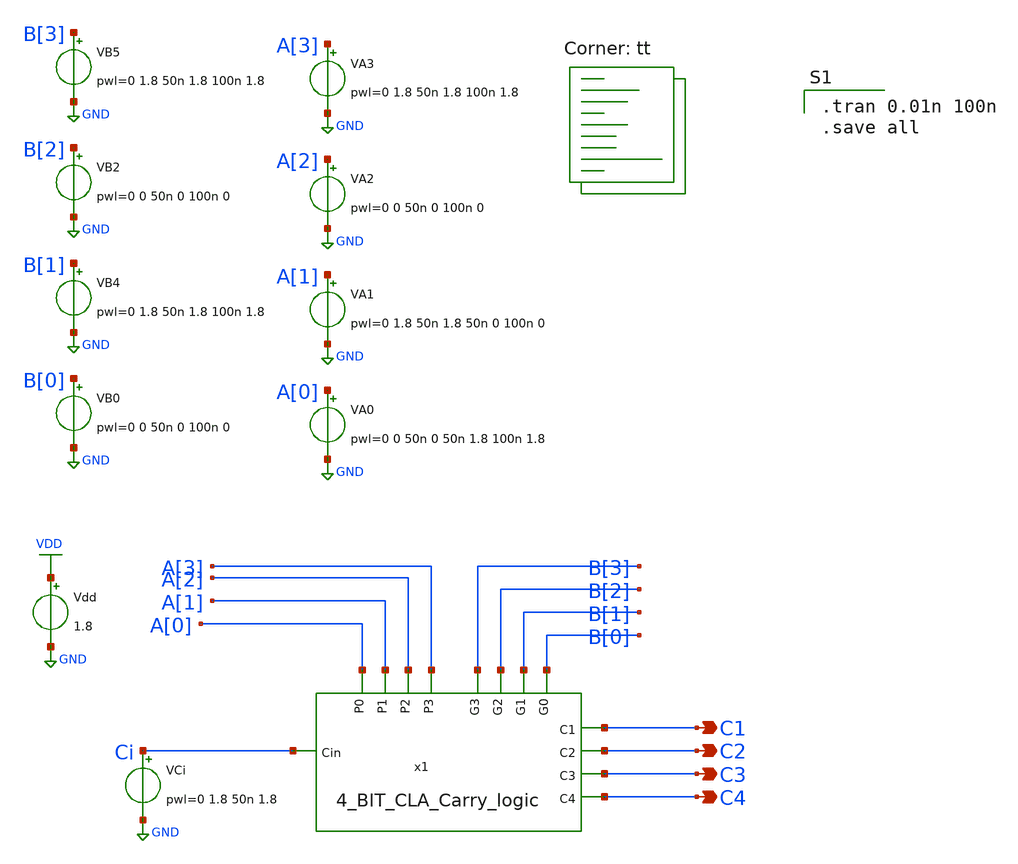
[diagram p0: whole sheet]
** sch_path: gates/cla logicsim.sch
**.subckt cla logicsim C4 C3 C2 C1
*.opin C4
*.opin C3
*.opin C2
*.opin C1
x1 A[1] B[1] A[3] A[0] A[2] B[2] B[3] Ci B[0] C1 C2 C3 C4 4_BIT_CLA_Carry_logic
VA3 A[3] GND pwl=0 1.8 50n 1.8 100n 1.8
VA2 A[2] GND pwl=0 0 50n 0 100n 0
VA1 A[1] GND pwl=0 1.8 50n 1.8 50n 0 100n 0
VA0 A[0] GND pwl=0 0 50n 0 50n 1.8 100n 1.8
VB5 B[3] GND pwl=0 1.8 50n 1.8 100n 1.8
VB2 B[2] GND pwl=0 0 50n 0 100n 0
VB4 B[1] GND pwl=0 1.8 50n 1.8 100n 1.8
VB0 B[0] GND pwl=0 0 50n 0 100n 0
VCi Ci GND pwl=0 1.8 50n 1.8
Vdd VDD GND 1.8
**** begin user architecture code
.lib $::SKYWATER_MODELS/sky130.lib.spice tt

.tran 0.01n 100n
.save all

**** end user architecture code
**.ends

* expanding   symbol:  4_BIT_CLA_Carry_logic.sym # of pins=13
** sym_path: gates/4_BIT_CLA_Carry_logic.sym
** sch_path: gates/4_BIT_CLA_Carry_logic.sch
.subckt 4_BIT_CLA_Carry_logic P1 G1 P3 P0 P2 G2 G3 Cin G0 C1 C2 C3 C4
*.ipin P0
*.ipin P1
*.ipin P2
*.ipin P3
*.ipin G0
*.ipin G1
*.ipin G2
*.ipin G3
*.ipin Cin
*.opin C1
*.opin C2
*.opin C3
*.opin C4
x5 Cin x5 P0 AND2
x6 G0 C1 x5 OR2
x7 G1 net1 net2 C2 OR3
x8 P1 net1 G0 AND2
x9 Cin net10 P0 P1 AND3
x1 G2 net3 net4 C3 net5 OR4
x2 P2 net3 G1 AND2
x3 P1 net11 P2 G0 AND3
x4 net12 net5 net13 net14 net15 AND4
x10 G3 net6 net7 net8 C4 net9 OR5
x12 P3 net6 G2 AND2
x13 net16 net17 net18 net19 AND3
x14 net20 net8 net21 net22 net23 AND4
x11 net24 net25 net26 net27 net28 net29 AND5
.ends


* expanding   symbol:  AND2.sym # of pins=3
** sym_path: gates/AND2.sym
** sch_path: gates/AND2.sch
.subckt AND2 A Y B
*.opin Y
*.ipin A
*.ipin B
x1 A net1 B NAND2_Gate
X2 net1 Y inv_vtc
.ends


* expanding   symbol:  OR2.sym # of pins=3
** sym_path: gates/OR2.sym
** sch_path: gates/OR2.sch
.subckt OR2 B Y A
*.ipin A
*.ipin B
*.opin Y
XM7 VDD B net2 VDD sky130_fd_pr__pfet_01v8 L=0.15 W=1 nf=1 ad='int((nf+1)/2) * W/nf * 0.29' as='int((nf+2)/2) * W/nf * 0.29'
+ pd='2*int((nf+1)/2) * (W/nf + 0.29)' ps='2*int((nf+2)/2) * (W/nf + 0.29)' nrd='0.29 / W' nrs='0.29 / W'
+ sa=0 sb=0 sd=0 mult=1 m=1
XM8 GND B net1 GND sky130_fd_pr__nfet_01v8 L=0.15 W=1 nf=1 ad='int((nf+1)/2) * W/nf * 0.29' as='int((nf+2)/2) * W/nf * 0.29'
+ pd='2*int((nf+1)/2) * (W/nf + 0.29)' ps='2*int((nf+2)/2) * (W/nf + 0.29)' nrd='0.29 / W' nrs='0.29 / W'
+ sa=0 sb=0 sd=0 mult=1 m=1
XM9 net2 A net1 VDD sky130_fd_pr__pfet_01v8 L=0.15 W=1 nf=1 ad='int((nf+1)/2) * W/nf * 0.29' as='int((nf+2)/2) * W/nf * 0.29'
+ pd='2*int((nf+1)/2) * (W/nf + 0.29)' ps='2*int((nf+2)/2) * (W/nf + 0.29)' nrd='0.29 / W' nrs='0.29 / W'
+ sa=0 sb=0 sd=0 mult=1 m=1
XM10 GND A net1 GND sky130_fd_pr__nfet_01v8 L=0.15 W=1 nf=1 ad='int((nf+1)/2) * W/nf * 0.29' as='int((nf+2)/2) * W/nf * 0.29'
+ pd='2*int((nf+1)/2) * (W/nf + 0.29)' ps='2*int((nf+2)/2) * (W/nf + 0.29)' nrd='0.29 / W' nrs='0.29 / W'
+ sa=0 sb=0 sd=0 mult=1 m=1
X1 net1 Y inv_vtc
.ends


* expanding   symbol:  OR3.sym # of pins=4
** sym_path: gates/OR3.sym
** sch_path: gates/OR3.sch
.subckt OR3 C B A Y
*.ipin A
*.ipin B
*.opin Y
*.ipin C
XM5 VDD C net3 VDD sky130_fd_pr__pfet_01v8 L=0.15 W=1 nf=1 ad='int((nf+1)/2) * W/nf * 0.29' as='int((nf+2)/2) * W/nf * 0.29'
+ pd='2*int((nf+1)/2) * (W/nf + 0.29)' ps='2*int((nf+2)/2) * (W/nf + 0.29)' nrd='0.29 / W' nrs='0.29 / W'
+ sa=0 sb=0 sd=0 mult=1 m=1
XM6 GND C net1 GND sky130_fd_pr__nfet_01v8 L=0.15 W=1 nf=1 ad='int((nf+1)/2) * W/nf * 0.29' as='int((nf+2)/2) * W/nf * 0.29'
+ pd='2*int((nf+1)/2) * (W/nf + 0.29)' ps='2*int((nf+2)/2) * (W/nf + 0.29)' nrd='0.29 / W' nrs='0.29 / W'
+ sa=0 sb=0 sd=0 mult=1 m=1
XM7 net3 B net2 VDD sky130_fd_pr__pfet_01v8 L=0.15 W=1 nf=1 ad='int((nf+1)/2) * W/nf * 0.29' as='int((nf+2)/2) * W/nf * 0.29'
+ pd='2*int((nf+1)/2) * (W/nf + 0.29)' ps='2*int((nf+2)/2) * (W/nf + 0.29)' nrd='0.29 / W' nrs='0.29 / W'
+ sa=0 sb=0 sd=0 mult=1 m=1
XM8 GND B net1 GND sky130_fd_pr__nfet_01v8 L=0.15 W=1 nf=1 ad='int((nf+1)/2) * W/nf * 0.29' as='int((nf+2)/2) * W/nf * 0.29'
+ pd='2*int((nf+1)/2) * (W/nf + 0.29)' ps='2*int((nf+2)/2) * (W/nf + 0.29)' nrd='0.29 / W' nrs='0.29 / W'
+ sa=0 sb=0 sd=0 mult=1 m=1
XM9 net2 A net1 VDD sky130_fd_pr__pfet_01v8 L=0.15 W=1 nf=1 ad='int((nf+1)/2) * W/nf * 0.29' as='int((nf+2)/2) * W/nf * 0.29'
+ pd='2*int((nf+1)/2) * (W/nf + 0.29)' ps='2*int((nf+2)/2) * (W/nf + 0.29)' nrd='0.29 / W' nrs='0.29 / W'
+ sa=0 sb=0 sd=0 mult=1 m=1
XM10 GND A net1 GND sky130_fd_pr__nfet_01v8 L=0.15 W=1 nf=1 ad='int((nf+1)/2) * W/nf * 0.29' as='int((nf+2)/2) * W/nf * 0.29'
+ pd='2*int((nf+1)/2) * (W/nf + 0.29)' ps='2*int((nf+2)/2) * (W/nf + 0.29)' nrd='0.29 / W' nrs='0.29 / W'
+ sa=0 sb=0 sd=0 mult=1 m=1
X1 net1 Y inv_vtc
.ends


* expanding   symbol:  AND3.sym # of pins=4
** sym_path: gates/AND3.sym
** sch_path: gates/AND3.sch
.subckt AND3 A Y B c
*.ipin A
*.ipin B
*.opin Y
*.ipin c
XM1 net1 A net2 GND sky130_fd_pr__nfet_01v8 L=0.15 W=1 nf=1 ad='int((nf+1)/2) * W/nf * 0.29' as='int((nf+2)/2) * W/nf * 0.29'
+ pd='2*int((nf+1)/2) * (W/nf + 0.29)' ps='2*int((nf+2)/2) * (W/nf + 0.29)' nrd='0.29 / W' nrs='0.29 / W'
+ sa=0 sb=0 sd=0 mult=1 m=1
XM2 net2 B net3 GND sky130_fd_pr__nfet_01v8 L=0.15 W=1 nf=1 ad='int((nf+1)/2) * W/nf * 0.29' as='int((nf+2)/2) * W/nf * 0.29'
+ pd='2*int((nf+1)/2) * (W/nf + 0.29)' ps='2*int((nf+2)/2) * (W/nf + 0.29)' nrd='0.29 / W' nrs='0.29 / W'
+ sa=0 sb=0 sd=0 mult=1 m=1
XM3 net1 A VDD VDD sky130_fd_pr__pfet_01v8 L=0.15 W=1 nf=1 ad='int((nf+1)/2) * W/nf * 0.29' as='int((nf+2)/2) * W/nf * 0.29'
+ pd='2*int((nf+1)/2) * (W/nf + 0.29)' ps='2*int((nf+2)/2) * (W/nf + 0.29)' nrd='0.29 / W' nrs='0.29 / W'
+ sa=0 sb=0 sd=0 mult=1 m=1
XM4 net1 B VDD VDD sky130_fd_pr__pfet_01v8 L=0.15 W=1 nf=1 ad='int((nf+1)/2) * W/nf * 0.29' as='int((nf+2)/2) * W/nf * 0.29'
+ pd='2*int((nf+1)/2) * (W/nf + 0.29)' ps='2*int((nf+2)/2) * (W/nf + 0.29)' nrd='0.29 / W' nrs='0.29 / W'
+ sa=0 sb=0 sd=0 mult=1 m=1
XM5 net1 c VDD VDD sky130_fd_pr__pfet_01v8 L=0.15 W=1 nf=1 ad='int((nf+1)/2) * W/nf * 0.29' as='int((nf+2)/2) * W/nf * 0.29'
+ pd='2*int((nf+1)/2) * (W/nf + 0.29)' ps='2*int((nf+2)/2) * (W/nf + 0.29)' nrd='0.29 / W' nrs='0.29 / W'
+ sa=0 sb=0 sd=0 mult=1 m=1
XM6 net3 c GND GND sky130_fd_pr__nfet_01v8 L=0.15 W=1 nf=1 ad='int((nf+1)/2) * W/nf * 0.29' as='int((nf+2)/2) * W/nf * 0.29'
+ pd='2*int((nf+1)/2) * (W/nf + 0.29)' ps='2*int((nf+2)/2) * (W/nf + 0.29)' nrd='0.29 / W' nrs='0.29 / W'
+ sa=0 sb=0 sd=0 mult=1 m=1
X1 net1 Y inv_vtc
.ends


* expanding   symbol:  OR4.sym # of pins=5
** sym_path: gates/OR4.sym
** sch_path: gates/OR4.sch
.subckt OR4 D C B Y A
*.ipin A
*.ipin B
*.opin Y
*.ipin C
*.ipin D
XM2 GND D net1 GND sky130_fd_pr__nfet_01v8 L=0.15 W=1 nf=1 ad='int((nf+1)/2) * W/nf * 0.29' as='int((nf+2)/2) * W/nf * 0.29'
+ pd='2*int((nf+1)/2) * (W/nf + 0.29)' ps='2*int((nf+2)/2) * (W/nf + 0.29)' nrd='0.29 / W' nrs='0.29 / W'
+ sa=0 sb=0 sd=0 mult=1 m=1
XM4 VDD D net4 VDD sky130_fd_pr__pfet_01v8 L=0.15 W=1 nf=1 ad='int((nf+1)/2) * W/nf * 0.29' as='int((nf+2)/2) * W/nf * 0.29'
+ pd='2*int((nf+1)/2) * (W/nf + 0.29)' ps='2*int((nf+2)/2) * (W/nf + 0.29)' nrd='0.29 / W' nrs='0.29 / W'
+ sa=0 sb=0 sd=0 mult=1 m=1
XM5 net4 C net3 VDD sky130_fd_pr__pfet_01v8 L=0.15 W=1 nf=1 ad='int((nf+1)/2) * W/nf * 0.29' as='int((nf+2)/2) * W/nf * 0.29'
+ pd='2*int((nf+1)/2) * (W/nf + 0.29)' ps='2*int((nf+2)/2) * (W/nf + 0.29)' nrd='0.29 / W' nrs='0.29 / W'
+ sa=0 sb=0 sd=0 mult=1 m=1
XM6 GND C net1 GND sky130_fd_pr__nfet_01v8 L=0.15 W=1 nf=1 ad='int((nf+1)/2) * W/nf * 0.29' as='int((nf+2)/2) * W/nf * 0.29'
+ pd='2*int((nf+1)/2) * (W/nf + 0.29)' ps='2*int((nf+2)/2) * (W/nf + 0.29)' nrd='0.29 / W' nrs='0.29 / W'
+ sa=0 sb=0 sd=0 mult=1 m=1
XM7 net3 B net2 VDD sky130_fd_pr__pfet_01v8 L=0.15 W=1 nf=1 ad='int((nf+1)/2) * W/nf * 0.29' as='int((nf+2)/2) * W/nf * 0.29'
+ pd='2*int((nf+1)/2) * (W/nf + 0.29)' ps='2*int((nf+2)/2) * (W/nf + 0.29)' nrd='0.29 / W' nrs='0.29 / W'
+ sa=0 sb=0 sd=0 mult=1 m=1
XM8 GND B net1 GND sky130_fd_pr__nfet_01v8 L=0.15 W=1 nf=1 ad='int((nf+1)/2) * W/nf * 0.29' as='int((nf+2)/2) * W/nf * 0.29'
+ pd='2*int((nf+1)/2) * (W/nf + 0.29)' ps='2*int((nf+2)/2) * (W/nf + 0.29)' nrd='0.29 / W' nrs='0.29 / W'
+ sa=0 sb=0 sd=0 mult=1 m=1
XM9 net2 A net1 VDD sky130_fd_pr__pfet_01v8 L=0.15 W=1 nf=1 ad='int((nf+1)/2) * W/nf * 0.29' as='int((nf+2)/2) * W/nf * 0.29'
+ pd='2*int((nf+1)/2) * (W/nf + 0.29)' ps='2*int((nf+2)/2) * (W/nf + 0.29)' nrd='0.29 / W' nrs='0.29 / W'
+ sa=0 sb=0 sd=0 mult=1 m=1
XM10 GND A net1 GND sky130_fd_pr__nfet_01v8 L=0.15 W=1 nf=1 ad='int((nf+1)/2) * W/nf * 0.29' as='int((nf+2)/2) * W/nf * 0.29'
+ pd='2*int((nf+1)/2) * (W/nf + 0.29)' ps='2*int((nf+2)/2) * (W/nf + 0.29)' nrd='0.29 / W' nrs='0.29 / W'
+ sa=0 sb=0 sd=0 mult=1 m=1
X2 net1 Y inv_vtc
.ends


* expanding   symbol:  AND4.sym # of pins=5
** sym_path: gates/AND4.sym
** sch_path: gates/AND4.sch
.subckt AND4 A Y B C D
*.ipin A
*.ipin B
*.opin Y
*.ipin C
*.ipin D
XM1 net1 A net2 GND sky130_fd_pr__nfet_01v8 L=0.15 W=1 nf=1 ad='int((nf+1)/2) * W/nf * 0.29' as='int((nf+2)/2) * W/nf * 0.29'
+ pd='2*int((nf+1)/2) * (W/nf + 0.29)' ps='2*int((nf+2)/2) * (W/nf + 0.29)' nrd='0.29 / W' nrs='0.29 / W'
+ sa=0 sb=0 sd=0 mult=1 m=1
XM2 net2 B net3 GND sky130_fd_pr__nfet_01v8 L=0.15 W=1 nf=1 ad='int((nf+1)/2) * W/nf * 0.29' as='int((nf+2)/2) * W/nf * 0.29'
+ pd='2*int((nf+1)/2) * (W/nf + 0.29)' ps='2*int((nf+2)/2) * (W/nf + 0.29)' nrd='0.29 / W' nrs='0.29 / W'
+ sa=0 sb=0 sd=0 mult=1 m=1
XM3 net1 A VDD VDD sky130_fd_pr__pfet_01v8 L=0.15 W=1 nf=1 ad='int((nf+1)/2) * W/nf * 0.29' as='int((nf+2)/2) * W/nf * 0.29'
+ pd='2*int((nf+1)/2) * (W/nf + 0.29)' ps='2*int((nf+2)/2) * (W/nf + 0.29)' nrd='0.29 / W' nrs='0.29 / W'
+ sa=0 sb=0 sd=0 mult=1 m=1
XM4 net1 B VDD VDD sky130_fd_pr__pfet_01v8 L=0.15 W=1 nf=1 ad='int((nf+1)/2) * W/nf * 0.29' as='int((nf+2)/2) * W/nf * 0.29'
+ pd='2*int((nf+1)/2) * (W/nf + 0.29)' ps='2*int((nf+2)/2) * (W/nf + 0.29)' nrd='0.29 / W' nrs='0.29 / W'
+ sa=0 sb=0 sd=0 mult=1 m=1
XM5 net1 C VDD VDD sky130_fd_pr__pfet_01v8 L=0.15 W=1 nf=1 ad='int((nf+1)/2) * W/nf * 0.29' as='int((nf+2)/2) * W/nf * 0.29'
+ pd='2*int((nf+1)/2) * (W/nf + 0.29)' ps='2*int((nf+2)/2) * (W/nf + 0.29)' nrd='0.29 / W' nrs='0.29 / W'
+ sa=0 sb=0 sd=0 mult=1 m=1
XM6 net3 C net4 GND sky130_fd_pr__nfet_01v8 L=0.15 W=1 nf=1 ad='int((nf+1)/2) * W/nf * 0.29' as='int((nf+2)/2) * W/nf * 0.29'
+ pd='2*int((nf+1)/2) * (W/nf + 0.29)' ps='2*int((nf+2)/2) * (W/nf + 0.29)' nrd='0.29 / W' nrs='0.29 / W'
+ sa=0 sb=0 sd=0 mult=1 m=1
XM7 net1 D VDD VDD sky130_fd_pr__pfet_01v8 L=0.15 W=1 nf=1 ad='int((nf+1)/2) * W/nf * 0.29' as='int((nf+2)/2) * W/nf * 0.29'
+ pd='2*int((nf+1)/2) * (W/nf + 0.29)' ps='2*int((nf+2)/2) * (W/nf + 0.29)' nrd='0.29 / W' nrs='0.29 / W'
+ sa=0 sb=0 sd=0 mult=1 m=1
XM8 net4 D GND GND sky130_fd_pr__nfet_01v8 L=0.15 W=1 nf=1 ad='int((nf+1)/2) * W/nf * 0.29' as='int((nf+2)/2) * W/nf * 0.29'
+ pd='2*int((nf+1)/2) * (W/nf + 0.29)' ps='2*int((nf+2)/2) * (W/nf + 0.29)' nrd='0.29 / W' nrs='0.29 / W'
+ sa=0 sb=0 sd=0 mult=1 m=1
X1 net1 Y inv_vtc
.ends


* expanding   symbol:  OR5.sym # of pins=6
** sym_path: gates/OR5.sym
** sch_path: gates/OR5.sch
.subckt OR5 E D C B Y A
*.ipin A
*.ipin B
*.opin Y
*.ipin C
*.ipin D
*.ipin E
XM1 GND E net1 GND sky130_fd_pr__nfet_01v8 L=0.15 W=1 nf=1 ad='int((nf+1)/2) * W/nf * 0.29' as='int((nf+2)/2) * W/nf * 0.29'
+ pd='2*int((nf+1)/2) * (W/nf + 0.29)' ps='2*int((nf+2)/2) * (W/nf + 0.29)' nrd='0.29 / W' nrs='0.29 / W'
+ sa=0 sb=0 sd=0 mult=1 m=1
XM2 GND D net1 GND sky130_fd_pr__nfet_01v8 L=0.15 W=1 nf=1 ad='int((nf+1)/2) * W/nf * 0.29' as='int((nf+2)/2) * W/nf * 0.29'
+ pd='2*int((nf+1)/2) * (W/nf + 0.29)' ps='2*int((nf+2)/2) * (W/nf + 0.29)' nrd='0.29 / W' nrs='0.29 / W'
+ sa=0 sb=0 sd=0 mult=1 m=1
XM3 VDD E VDD VDD sky130_fd_pr__pfet_01v8 L=0.15 W=1 nf=1 ad='int((nf+1)/2) * W/nf * 0.29' as='int((nf+2)/2) * W/nf * 0.29'
+ pd='2*int((nf+1)/2) * (W/nf + 0.29)' ps='2*int((nf+2)/2) * (W/nf + 0.29)' nrd='0.29 / W' nrs='0.29 / W'
+ sa=0 sb=0 sd=0 mult=1 m=1
XM4 VDD D net4 VDD sky130_fd_pr__pfet_01v8 L=0.15 W=1 nf=1 ad='int((nf+1)/2) * W/nf * 0.29' as='int((nf+2)/2) * W/nf * 0.29'
+ pd='2*int((nf+1)/2) * (W/nf + 0.29)' ps='2*int((nf+2)/2) * (W/nf + 0.29)' nrd='0.29 / W' nrs='0.29 / W'
+ sa=0 sb=0 sd=0 mult=1 m=1
XM5 net4 C net3 VDD sky130_fd_pr__pfet_01v8 L=0.15 W=1 nf=1 ad='int((nf+1)/2) * W/nf * 0.29' as='int((nf+2)/2) * W/nf * 0.29'
+ pd='2*int((nf+1)/2) * (W/nf + 0.29)' ps='2*int((nf+2)/2) * (W/nf + 0.29)' nrd='0.29 / W' nrs='0.29 / W'
+ sa=0 sb=0 sd=0 mult=1 m=1
XM6 GND C net1 GND sky130_fd_pr__nfet_01v8 L=0.15 W=1 nf=1 ad='int((nf+1)/2) * W/nf * 0.29' as='int((nf+2)/2) * W/nf * 0.29'
+ pd='2*int((nf+1)/2) * (W/nf + 0.29)' ps='2*int((nf+2)/2) * (W/nf + 0.29)' nrd='0.29 / W' nrs='0.29 / W'
+ sa=0 sb=0 sd=0 mult=1 m=1
XM7 net3 B net2 VDD sky130_fd_pr__pfet_01v8 L=0.15 W=1 nf=1 ad='int((nf+1)/2) * W/nf * 0.29' as='int((nf+2)/2) * W/nf * 0.29'
+ pd='2*int((nf+1)/2) * (W/nf + 0.29)' ps='2*int((nf+2)/2) * (W/nf + 0.29)' nrd='0.29 / W' nrs='0.29 / W'
+ sa=0 sb=0 sd=0 mult=1 m=1
XM8 GND B net1 GND sky130_fd_pr__nfet_01v8 L=0.15 W=1 nf=1 ad='int((nf+1)/2) * W/nf * 0.29' as='int((nf+2)/2) * W/nf * 0.29'
+ pd='2*int((nf+1)/2) * (W/nf + 0.29)' ps='2*int((nf+2)/2) * (W/nf + 0.29)' nrd='0.29 / W' nrs='0.29 / W'
+ sa=0 sb=0 sd=0 mult=1 m=1
XM9 net2 A net1 VDD sky130_fd_pr__pfet_01v8 L=0.15 W=1 nf=1 ad='int((nf+1)/2) * W/nf * 0.29' as='int((nf+2)/2) * W/nf * 0.29'
+ pd='2*int((nf+1)/2) * (W/nf + 0.29)' ps='2*int((nf+2)/2) * (W/nf + 0.29)' nrd='0.29 / W' nrs='0.29 / W'
+ sa=0 sb=0 sd=0 mult=1 m=1
XM10 GND A net1 GND sky130_fd_pr__nfet_01v8 L=0.15 W=1 nf=1 ad='int((nf+1)/2) * W/nf * 0.29' as='int((nf+2)/2) * W/nf * 0.29'
+ pd='2*int((nf+1)/2) * (W/nf + 0.29)' ps='2*int((nf+2)/2) * (W/nf + 0.29)' nrd='0.29 / W' nrs='0.29 / W'
+ sa=0 sb=0 sd=0 mult=1 m=1
X2 net1 Y inv_vtc
.ends


* expanding   symbol:  AND5.sym # of pins=6
** sym_path: gates/AND5.sym
** sch_path: gates/AND5.sch
.subckt AND5 A Y B C D E
*.ipin A
*.ipin B
*.opin Y
*.ipin C
*.ipin D
*.ipin E
XM1 net1 A net2 GND sky130_fd_pr__nfet_01v8 L=0.15 W=1 nf=1 ad='int((nf+1)/2) * W/nf * 0.29' as='int((nf+2)/2) * W/nf * 0.29'
+ pd='2*int((nf+1)/2) * (W/nf + 0.29)' ps='2*int((nf+2)/2) * (W/nf + 0.29)' nrd='0.29 / W' nrs='0.29 / W'
+ sa=0 sb=0 sd=0 mult=1 m=1
XM2 net2 B net3 GND sky130_fd_pr__nfet_01v8 L=0.15 W=1 nf=1 ad='int((nf+1)/2) * W/nf * 0.29' as='int((nf+2)/2) * W/nf * 0.29'
+ pd='2*int((nf+1)/2) * (W/nf + 0.29)' ps='2*int((nf+2)/2) * (W/nf + 0.29)' nrd='0.29 / W' nrs='0.29 / W'
+ sa=0 sb=0 sd=0 mult=1 m=1
XM3 net1 A VDD VDD sky130_fd_pr__pfet_01v8 L=0.15 W=1 nf=1 ad='int((nf+1)/2) * W/nf * 0.29' as='int((nf+2)/2) * W/nf * 0.29'
+ pd='2*int((nf+1)/2) * (W/nf + 0.29)' ps='2*int((nf+2)/2) * (W/nf + 0.29)' nrd='0.29 / W' nrs='0.29 / W'
+ sa=0 sb=0 sd=0 mult=1 m=1
XM4 net1 B VDD VDD sky130_fd_pr__pfet_01v8 L=0.15 W=1 nf=1 ad='int((nf+1)/2) * W/nf * 0.29' as='int((nf+2)/2) * W/nf * 0.29'
+ pd='2*int((nf+1)/2) * (W/nf + 0.29)' ps='2*int((nf+2)/2) * (W/nf + 0.29)' nrd='0.29 / W' nrs='0.29 / W'
+ sa=0 sb=0 sd=0 mult=1 m=1
XM5 net1 C VDD VDD sky130_fd_pr__pfet_01v8 L=0.15 W=1 nf=1 ad='int((nf+1)/2) * W/nf * 0.29' as='int((nf+2)/2) * W/nf * 0.29'
+ pd='2*int((nf+1)/2) * (W/nf + 0.29)' ps='2*int((nf+2)/2) * (W/nf + 0.29)' nrd='0.29 / W' nrs='0.29 / W'
+ sa=0 sb=0 sd=0 mult=1 m=1
XM6 net3 C net4 GND sky130_fd_pr__nfet_01v8 L=0.15 W=1 nf=1 ad='int((nf+1)/2) * W/nf * 0.29' as='int((nf+2)/2) * W/nf * 0.29'
+ pd='2*int((nf+1)/2) * (W/nf + 0.29)' ps='2*int((nf+2)/2) * (W/nf + 0.29)' nrd='0.29 / W' nrs='0.29 / W'
+ sa=0 sb=0 sd=0 mult=1 m=1
XM7 net1 D VDD VDD sky130_fd_pr__pfet_01v8 L=0.15 W=1 nf=1 ad='int((nf+1)/2) * W/nf * 0.29' as='int((nf+2)/2) * W/nf * 0.29'
+ pd='2*int((nf+1)/2) * (W/nf + 0.29)' ps='2*int((nf+2)/2) * (W/nf + 0.29)' nrd='0.29 / W' nrs='0.29 / W'
+ sa=0 sb=0 sd=0 mult=1 m=1
XM8 net4 D GND GND sky130_fd_pr__nfet_01v8 L=0.15 W=1 nf=1 ad='int((nf+1)/2) * W/nf * 0.29' as='int((nf+2)/2) * W/nf * 0.29'
+ pd='2*int((nf+1)/2) * (W/nf + 0.29)' ps='2*int((nf+2)/2) * (W/nf + 0.29)' nrd='0.29 / W' nrs='0.29 / W'
+ sa=0 sb=0 sd=0 mult=1 m=1
XM9 net1 E VDD VDD sky130_fd_pr__pfet_01v8 L=0.15 W=1 nf=1 ad='int((nf+1)/2) * W/nf * 0.29' as='int((nf+2)/2) * W/nf * 0.29'
+ pd='2*int((nf+1)/2) * (W/nf + 0.29)' ps='2*int((nf+2)/2) * (W/nf + 0.29)' nrd='0.29 / W' nrs='0.29 / W'
+ sa=0 sb=0 sd=0 mult=1 m=1
XM10 GND E GND GND sky130_fd_pr__nfet_01v8 L=0.15 W=1 nf=1 ad='int((nf+1)/2) * W/nf * 0.29' as='int((nf+2)/2) * W/nf * 0.29'
+ pd='2*int((nf+1)/2) * (W/nf + 0.29)' ps='2*int((nf+2)/2) * (W/nf + 0.29)' nrd='0.29 / W' nrs='0.29 / W'
+ sa=0 sb=0 sd=0 mult=1 m=1
X1 net1 Y inv_vtc
.ends


* expanding   symbol:  NAND2_Gate.sym # of pins=3
** sym_path: gates/NAND2_Gate.sym
** sch_path: gates/NAND2_Gate.sch
.subckt NAND2_Gate A Y B
*.ipin A
*.ipin B
*.opin Y
XM1 Y A net1 GND sky130_fd_pr__nfet_01v8 L=0.15 W=1 nf=1 ad='int((nf+1)/2) * W/nf * 0.29' as='int((nf+2)/2) * W/nf * 0.29'
+ pd='2*int((nf+1)/2) * (W/nf + 0.29)' ps='2*int((nf+2)/2) * (W/nf + 0.29)' nrd='0.29 / W' nrs='0.29 / W'
+ sa=0 sb=0 sd=0 mult=1 m=1
XM2 net1 B GND GND sky130_fd_pr__nfet_01v8 L=0.15 W=1 nf=1 ad='int((nf+1)/2) * W/nf * 0.29' as='int((nf+2)/2) * W/nf * 0.29'
+ pd='2*int((nf+1)/2) * (W/nf + 0.29)' ps='2*int((nf+2)/2) * (W/nf + 0.29)' nrd='0.29 / W' nrs='0.29 / W'
+ sa=0 sb=0 sd=0 mult=1 m=1
XM3 Y A VDD VDD sky130_fd_pr__pfet_01v8 L=0.15 W=1 nf=1 ad='int((nf+1)/2) * W/nf * 0.29' as='int((nf+2)/2) * W/nf * 0.29'
+ pd='2*int((nf+1)/2) * (W/nf + 0.29)' ps='2*int((nf+2)/2) * (W/nf + 0.29)' nrd='0.29 / W' nrs='0.29 / W'
+ sa=0 sb=0 sd=0 mult=1 m=1
XM4 Y B VDD VDD sky130_fd_pr__pfet_01v8 L=0.15 W=1 nf=1 ad='int((nf+1)/2) * W/nf * 0.29' as='int((nf+2)/2) * W/nf * 0.29'
+ pd='2*int((nf+1)/2) * (W/nf + 0.29)' ps='2*int((nf+2)/2) * (W/nf + 0.29)' nrd='0.29 / W' nrs='0.29 / W'
+ sa=0 sb=0 sd=0 mult=1 m=1
.ends


* expanding   symbol:  /home/apn/test_xschem_sky130/inv_vtc.sym # of pins=2
** sym_path: gates/inv_vtc.sym
** sch_path: gates/inv_vtc.sch
.subckt inv_vtc A Y
*.ipin A
*.opin Y
XM1 Y A VDD VDD sky130_fd_pr__pfet_01v8 L=0.15 W=2 nf=1 ad='int((nf+1)/2) * W/nf * 0.29' as='int((nf+2)/2) * W/nf * 0.29'
+ pd='2*int((nf+1)/2) * (W/nf + 0.29)' ps='2*int((nf+2)/2) * (W/nf + 0.29)' nrd='0.29 / W' nrs='0.29 / W'
+ sa=0 sb=0 sd=0 mult=1 m=1
XM2 Y A GND GND sky130_fd_pr__nfet_01v8 L=0.15 W=1 nf=1 ad='int((nf+1)/2) * W/nf * 0.29' as='int((nf+2)/2) * W/nf * 0.29'
+ pd='2*int((nf+1)/2) * (W/nf + 0.29)' ps='2*int((nf+2)/2) * (W/nf + 0.29)' nrd='0.29 / W' nrs='0.29 / W'
+ sa=0 sb=0 sd=0 mult=1 m=1
.ends

.GLOBAL GND
.GLOBAL VDD
.end
